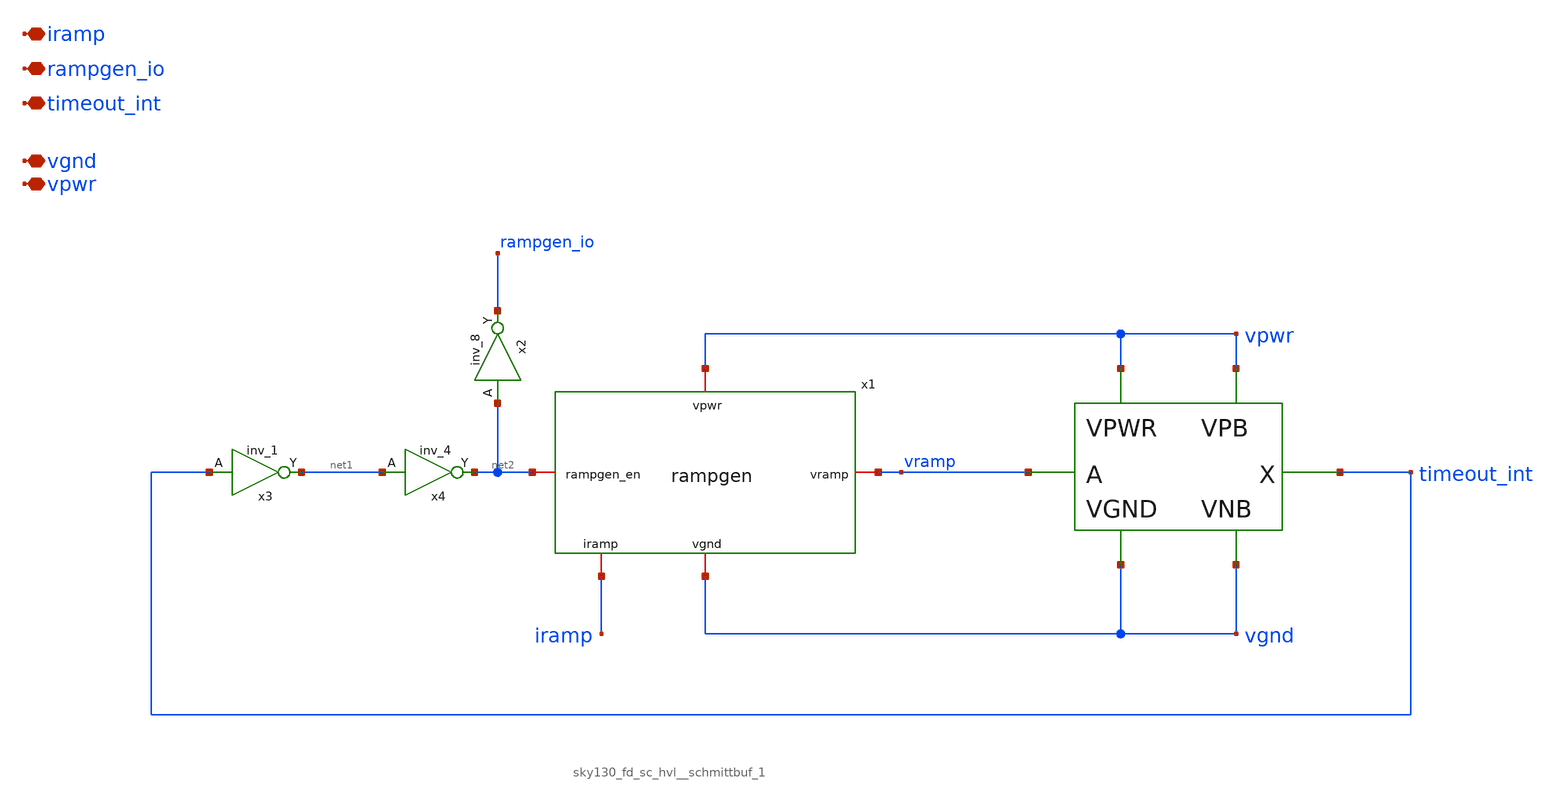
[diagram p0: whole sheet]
** sch_path: images/iic-osic-tools/addons/examples/Open-PMIC-tapeout/xschem/oscillator.sch
**.subckt oscillator iramp rampgen_io timeout_int vgnd vpwr
*.iopin iramp
*.iopin rampgen_io
*.iopin timeout_int
*.iopin vgnd
*.iopin vpwr
x4 net1 vgnd vgnd vpwr vpwr net2 sky130_fd_sc_hvl__inv_4
x1 vpwr vgnd iramp vramp net2 rampgen
x3 timeout_int vgnd vgnd vpwr vpwr net1 sky130_fd_sc_hvl__inv_1
x5 vramp vgnd vgnd vpwr vpwr timeout_int sky130_fd_sc_hvl__schmittbuf_1
x2 net2 vgnd vgnd vpwr vpwr rampgen_io sky130_fd_sc_hvl__inv_8
**** begin user architecture code


.include /usr/share/pdk/sky130A/libs.ref/sky130_fd_sc_hvl/spice/sky130_fd_sc_hvl.spice


**** end user architecture code
**.ends
.end
